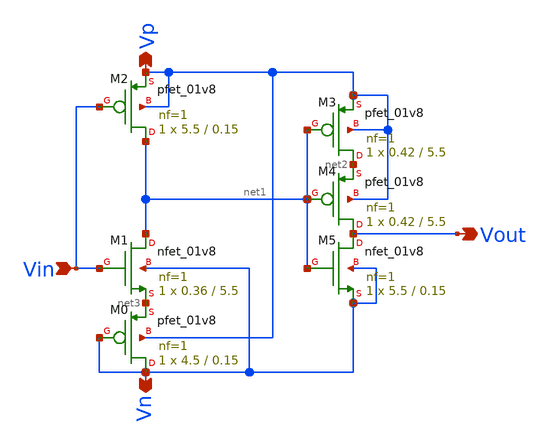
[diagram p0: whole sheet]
** sch_path: xschem/Vth_sch/Symbol/th14.sch
**.subckt th14 Vout Vn Vp Vin
*.opin Vout
*.opin Vn
*.opin Vp
*.ipin Vin
XM3 net2 net1 Vp Vp sky130_fd_pr__pfet_01v8 L=5.5 W=0.42 nf=1 ad='int((nf+1)/2) * W/nf * 0.29' as='int((nf+2)/2) * W/nf * 0.29'
+ pd='2*int((nf+1)/2) * (W/nf + 0.29)' ps='2*int((nf+2)/2) * (W/nf + 0.29)' nrd='0.29 / W' nrs='0.29 / W'
+ sa=0 sb=0 sd=0 mult=1 m=1
XM4 Vout net1 net2 Vp sky130_fd_pr__pfet_01v8 L=5.5 W=0.42 nf=1 ad='int((nf+1)/2) * W/nf * 0.29' as='int((nf+2)/2) * W/nf * 0.29'
+ pd='2*int((nf+1)/2) * (W/nf + 0.29)' ps='2*int((nf+2)/2) * (W/nf + 0.29)' nrd='0.29 / W' nrs='0.29 / W'
+ sa=0 sb=0 sd=0 mult=1 m=1
XM5 Vout net1 Vn Vn sky130_fd_pr__nfet_01v8 L=0.15 W=5.5 nf=1 ad='int((nf+1)/2) * W/nf * 0.29' as='int((nf+2)/2) * W/nf * 0.29'
+ pd='2*int((nf+1)/2) * (W/nf + 0.29)' ps='2*int((nf+2)/2) * (W/nf + 0.29)' nrd='0.29 / W' nrs='0.29 / W'
+ sa=0 sb=0 sd=0 mult=1 m=1
XM2 net1 Vin Vp Vp sky130_fd_pr__pfet_01v8 L=0.15 W=5.5 nf=1 ad='int((nf+1)/2) * W/nf * 0.29' as='int((nf+2)/2) * W/nf * 0.29'
+ pd='2*int((nf+1)/2) * (W/nf + 0.29)' ps='2*int((nf+2)/2) * (W/nf + 0.29)' nrd='0.29 / W' nrs='0.29 / W'
+ sa=0 sb=0 sd=0 mult=1 m=1
XM1 net1 Vin net3 Vn sky130_fd_pr__nfet_01v8 L=5.5 W=0.36 nf=1 ad='int((nf+1)/2) * W/nf * 0.29' as='int((nf+2)/2) * W/nf * 0.29'
+ pd='2*int((nf+1)/2) * (W/nf + 0.29)' ps='2*int((nf+2)/2) * (W/nf + 0.29)' nrd='0.29 / W' nrs='0.29 / W'
+ sa=0 sb=0 sd=0 mult=1 m=1
XM0 Vn Vn net3 Vp sky130_fd_pr__pfet_01v8 L=0.15 W=4.5 nf=1 ad='int((nf+1)/2) * W/nf * 0.29' as='int((nf+2)/2) * W/nf * 0.29'
+ pd='2*int((nf+1)/2) * (W/nf + 0.29)' ps='2*int((nf+2)/2) * (W/nf + 0.29)' nrd='0.29 / W' nrs='0.29 / W'
+ sa=0 sb=0 sd=0 mult=1 m=1
**.ends
.end
